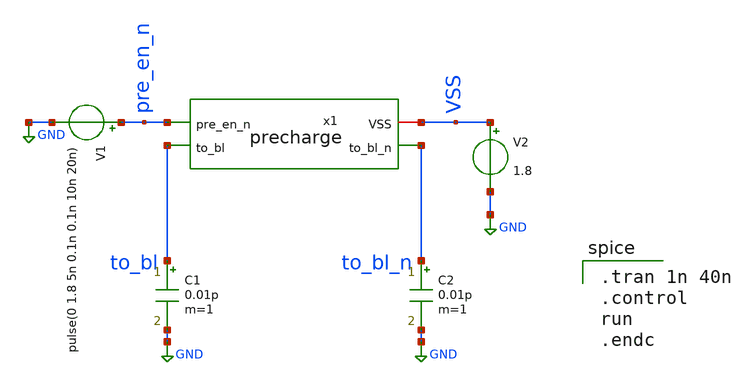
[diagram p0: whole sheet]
** sch_path: precharge_test.sch
**.subckt precharge_test
x1 VSS to_bl_n to_bl pre_en_n precharge
V1 pre_en_n GND pulse(0 1.8 5n 0.1n 0.1n 10n 20n)
V2 VSS GND 1.8
C1 to_bl GND 0.01p m=1
C2 to_bl_n GND 0.01p m=1
**** begin user architecture code
 .lib $::SKYWATER_MODELS/sky130.lib.spice tt

.tran 1n 40n
.control
run
.endc

**** end user architecture code
**.ends

* expanding   symbol:  /home/ee431/workspace/proj_4x4SRAM/precharge.sym # of pins=4
** sym_path: precharge.sym
** sch_path: precharge.sch
.subckt precharge VSS to_bl_n to_bl pre_en_n
*.ipin pre_en_n
*.opin to_bl
*.opin to_bl_n
*.iopin VSS
XM1 to_bl_n pre_en_n VSS VSS sky130_fd_pr__pfet_01v8 L=0.25 W=0.5 nf=1 ad='int((nf+1)/2) * W/nf * 0.29'
+ as='int((nf+2)/2) * W/nf * 0.29' pd='2*int((nf+1)/2) * (W/nf + 0.29)' ps='2*int((nf+2)/2) * (W/nf + 0.29)'
+ nrd='0.29 / W' nrs='0.29 / W' sa=0 sb=0 sd=0 mult=1 m=1
XM2 to_bl pre_en_n VSS VSS sky130_fd_pr__pfet_01v8 L=0.25 W=0.5 nf=1 ad='int((nf+1)/2) * W/nf * 0.29'
+ as='int((nf+2)/2) * W/nf * 0.29' pd='2*int((nf+1)/2) * (W/nf + 0.29)' ps='2*int((nf+2)/2) * (W/nf + 0.29)'
+ nrd='0.29 / W' nrs='0.29 / W' sa=0 sb=0 sd=0 mult=1 m=1
.ends

.GLOBAL GND
.end
